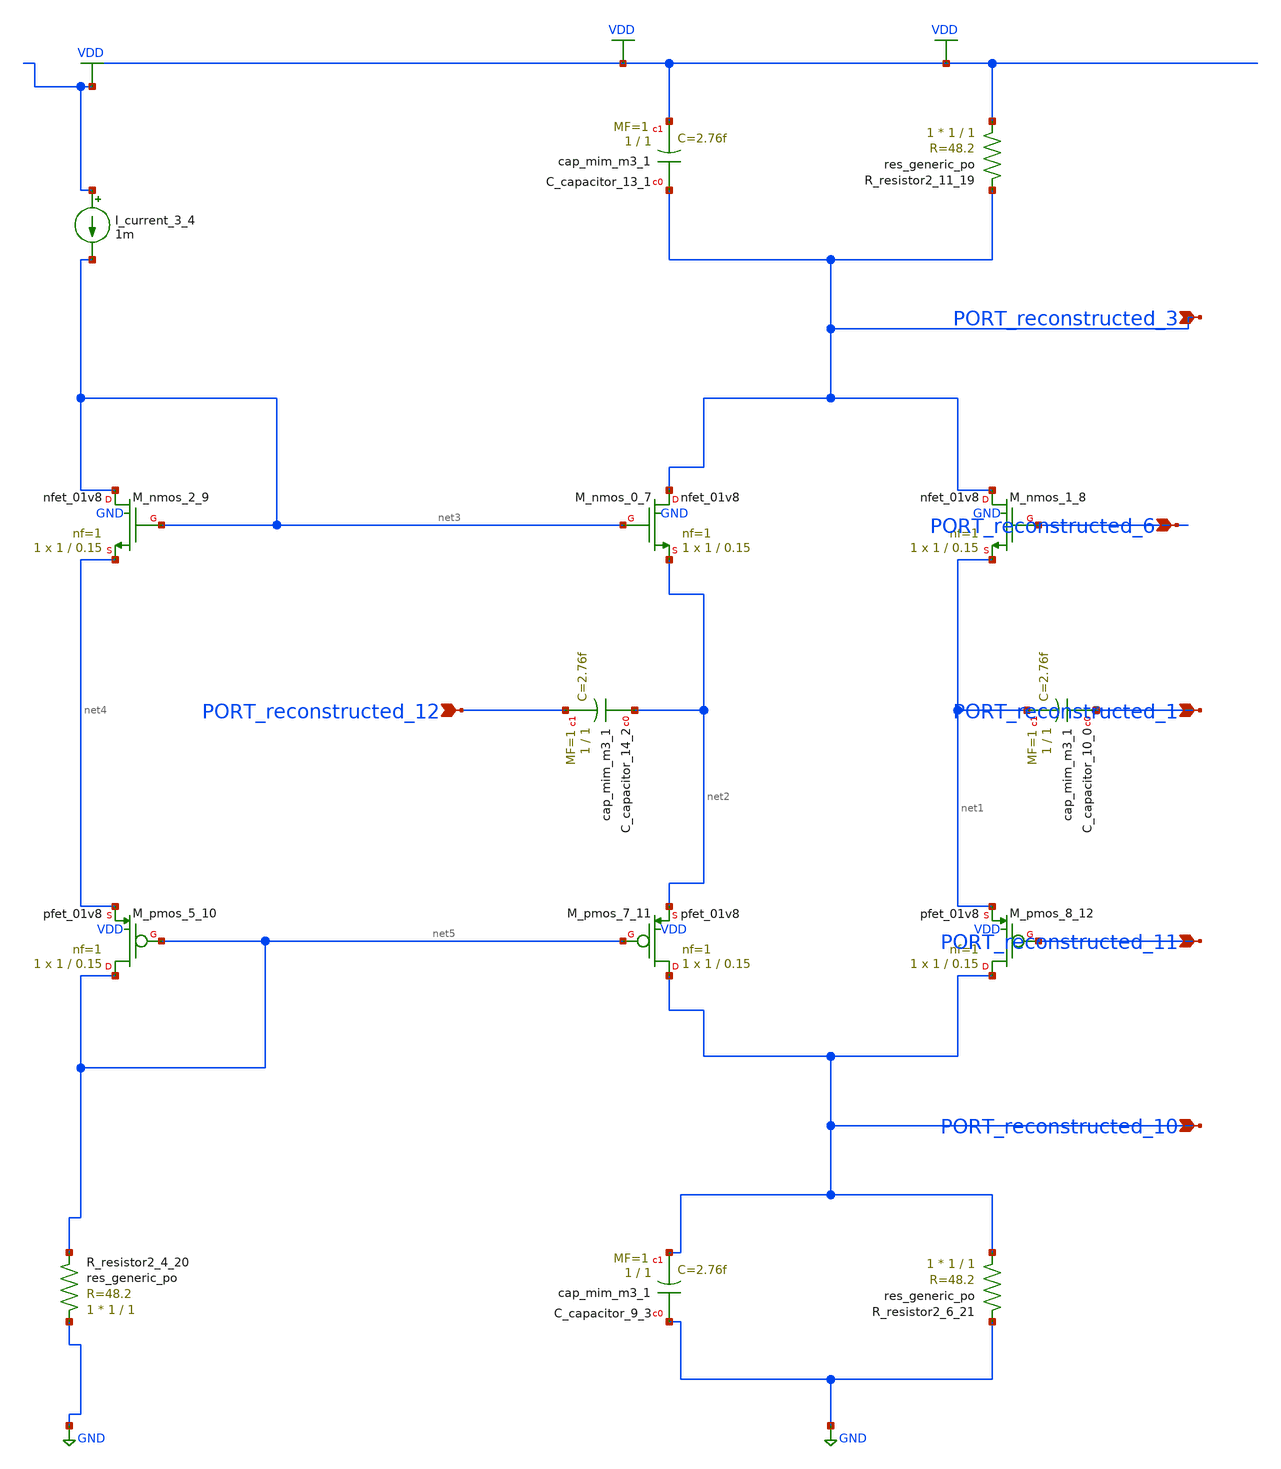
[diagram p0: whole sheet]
** sch_path: schematics/10_1109_ACCESS_2020_2989192_08_003.sch
**.subckt 10_1109_ACCESS_2020_2989192_08_003 PORT_reconstructed_1 PORT_reconstructed_3
*+ PORT_reconstructed_11 PORT_reconstructed_6 PORT_reconstructed_10 PORT_reconstructed_12
*.ipin PORT_reconstructed_1
*.ipin PORT_reconstructed_3
*.ipin PORT_reconstructed_11
*.ipin PORT_reconstructed_6
*.ipin PORT_reconstructed_10
*.ipin PORT_reconstructed_12
XC_capacitor_10_0 PORT_reconstructed_1 net1 sky130_fd_pr__cap_mim_m3_1 W=1 L=1 MF=1 m=1
XC_capacitor_13_1 PORT_reconstructed_3 VDD sky130_fd_pr__cap_mim_m3_1 W=1 L=1 MF=1 m=1
XC_capacitor_14_2 net2 PORT_reconstructed_12 sky130_fd_pr__cap_mim_m3_1 W=1 L=1 MF=1 m=1
XC_capacitor_9_3 GND PORT_reconstructed_10 sky130_fd_pr__cap_mim_m3_1 W=1 L=1 MF=1 m=1
I_current_3_4 VDD net3 1m
XM_nmos_0_7 PORT_reconstructed_3 net3 net2 GND sky130_fd_pr__nfet_01v8 L=0.15 W=1 nf=1 ad='int((1 + 1)/2) * 1 / 1 * 0.29'
+ as='int((1 + 2)/2) * 1 / 1 * 0.29' pd='2*int((1 + 1)/2) * (1 / 1 + 0.29)' ps='2*int((1 + 2)/2) * (1 / 1 + 0.29)'
+ nrd='0.29 / 1 ' nrs='0.29 / 1 ' sa=0 sb=0 sd=0 mult=1 m=1
XM_nmos_1_8 PORT_reconstructed_3 PORT_reconstructed_6 net1 GND sky130_fd_pr__nfet_01v8 L=0.15 W=1 nf=1
+ ad='int((1 + 1)/2) * 1 / 1 * 0.29' as='int((1 + 2)/2) * 1 / 1 * 0.29' pd='2*int((1 + 1)/2) * (1 / 1 + 0.29)'
+ ps='2*int((1 + 2)/2) * (1 / 1 + 0.29)' nrd='0.29 / 1 ' nrs='0.29 / 1 ' sa=0 sb=0 sd=0 mult=1 m=1
XM_nmos_2_9 net3 net3 net4 GND sky130_fd_pr__nfet_01v8 L=0.15 W=1 nf=1 ad='int((1 + 1)/2) * 1 / 1 * 0.29'
+ as='int((1 + 2)/2) * 1 / 1 * 0.29' pd='2*int((1 + 1)/2) * (1 / 1 + 0.29)' ps='2*int((1 + 2)/2) * (1 / 1 + 0.29)'
+ nrd='0.29 / 1 ' nrs='0.29 / 1 ' sa=0 sb=0 sd=0 mult=1 m=1
XM_pmos_5_10 net5 net5 net4 VDD sky130_fd_pr__pfet_01v8 L=0.15 W=1 nf=1 ad='int((1 + 1)/2) * 1 / 1 * 0.29'
+ as='int((1 + 2)/2) * 1 / 1 * 0.29' pd='2*int((1 + 1)/2) * (1 / 1 + 0.29)' ps='2*int((1 + 2)/2) * (1 / 1 + 0.29)'
+ nrd='0.29 / 1 ' nrs='0.29 / 1 ' sa=0 sb=0 sd=0 mult=1 m=1
XM_pmos_7_11 PORT_reconstructed_10 net5 net2 VDD sky130_fd_pr__pfet_01v8 L=0.15 W=1 nf=1 ad='int((1 + 1)/2) * 1 / 1 * 0.29'
+ as='int((1 + 2)/2) * 1 / 1 * 0.29' pd='2*int((1 + 1)/2) * (1 / 1 + 0.29)' ps='2*int((1 + 2)/2) * (1 / 1 + 0.29)'
+ nrd='0.29 / 1 ' nrs='0.29 / 1 ' sa=0 sb=0 sd=0 mult=1 m=1
XM_pmos_8_12 PORT_reconstructed_10 PORT_reconstructed_11 net1 VDD sky130_fd_pr__pfet_01v8 L=0.15 W=1
+ nf=1 ad='int((1 + 1)/2) * 1 / 1 * 0.29' as='int((1 + 2)/2) * 1 / 1 * 0.29' pd='2*int((1 + 1)/2) * (1 / 1 + 0.29)'
+ ps='2*int((1 + 2)/2) * (1 / 1 + 0.29)' nrd='0.29 / 1 ' nrs='0.29 / 1 ' sa=0 sb=0 sd=0 mult=1 m=1
XR_resistor2_11_19 VDD PORT_reconstructed_3 sky130_fd_pr__res_generic_po W=1 L=1 m=1
XR_resistor2_4_20 GND net5 sky130_fd_pr__res_generic_po W=1 L=1 m=1
XR_resistor2_6_21 PORT_reconstructed_10 GND sky130_fd_pr__res_generic_po W=1 L=1 m=1
**.ends
.GLOBAL GND
.GLOBAL VDD
.end
